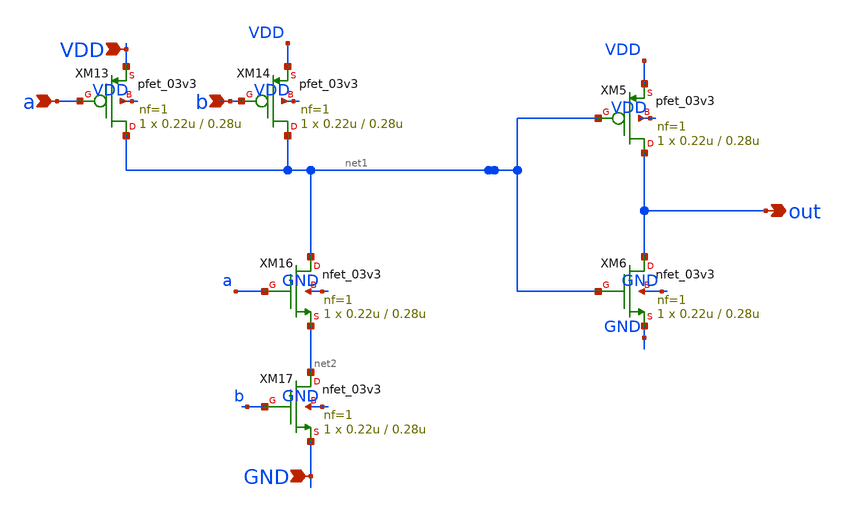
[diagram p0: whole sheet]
** sch_path: blocks/dsp-fft/sch/AND2.sch
**.subckt AND2 a out b VDD GND
*.ipin a
*.opin out
*.ipin b
*.ipin VDD
*.ipin GND
XM5 out net1 VDD VDD pfet_03v3 L=0.28u W=0.22u nf=1 ad='int((nf+1)/2) * W/nf * 0.18u' as='int((nf+2)/2) * W/nf * 0.18u'
+ pd='2*int((nf+1)/2) * (W/nf + 0.18u)' ps='2*int((nf+2)/2) * (W/nf + 0.18u)' nrd='0.18u / W' nrs='0.18u / W'
+ sa=0 sb=0 sd=0 m=1
XM6 out net1 GND GND nfet_03v3 L=0.28u W=0.22u nf=1 ad='int((nf+1)/2) * W/nf * 0.18u' as='int((nf+2)/2) * W/nf * 0.18u'
+ pd='2*int((nf+1)/2) * (W/nf + 0.18u)' ps='2*int((nf+2)/2) * (W/nf + 0.18u)' nrd='0.18u / W' nrs='0.18u / W'
+ sa=0 sb=0 sd=0 m=1
XM13 net1 a VDD VDD pfet_03v3 L=0.28u W=0.22u nf=1 ad='int((nf+1)/2) * W/nf * 0.18u' as='int((nf+2)/2) * W/nf * 0.18u'
+ pd='2*int((nf+1)/2) * (W/nf + 0.18u)' ps='2*int((nf+2)/2) * (W/nf + 0.18u)' nrd='0.18u / W' nrs='0.18u / W'
+ sa=0 sb=0 sd=0 m=1
XM14 net1 b VDD VDD pfet_03v3 L=0.28u W=0.22u nf=1 ad='int((nf+1)/2) * W/nf * 0.18u' as='int((nf+2)/2) * W/nf * 0.18u'
+ pd='2*int((nf+1)/2) * (W/nf + 0.18u)' ps='2*int((nf+2)/2) * (W/nf + 0.18u)' nrd='0.18u / W' nrs='0.18u / W'
+ sa=0 sb=0 sd=0 m=1
XM16 net1 a net2 GND nfet_03v3 L=0.28u W=0.22u nf=1 ad='int((nf+1)/2) * W/nf * 0.18u' as='int((nf+2)/2) * W/nf * 0.18u'
+ pd='2*int((nf+1)/2) * (W/nf + 0.18u)' ps='2*int((nf+2)/2) * (W/nf + 0.18u)' nrd='0.18u / W' nrs='0.18u / W'
+ sa=0 sb=0 sd=0 m=1
XM17 net2 b GND GND nfet_03v3 L=0.28u W=0.22u nf=1 ad='int((nf+1)/2) * W/nf * 0.18u' as='int((nf+2)/2) * W/nf * 0.18u'
+ pd='2*int((nf+1)/2) * (W/nf + 0.18u)' ps='2*int((nf+2)/2) * (W/nf + 0.18u)' nrd='0.18u / W' nrs='0.18u / W'
+ sa=0 sb=0 sd=0 m=1
**.ends
.end
